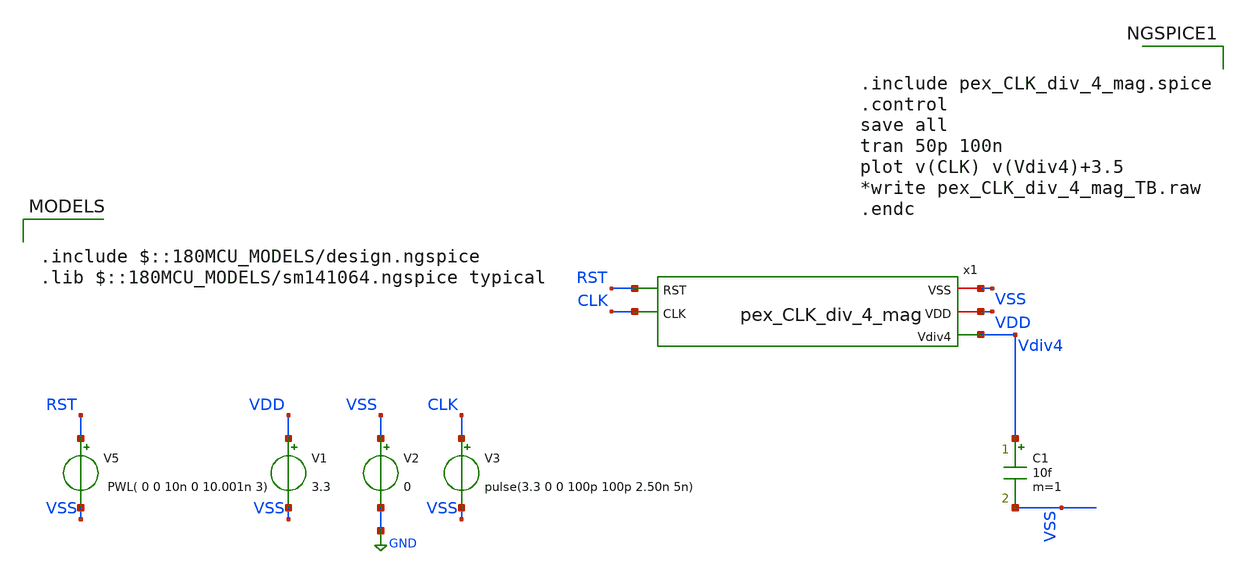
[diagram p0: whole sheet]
** sch_path: Clock_Generator_PAKISTAN_02/Schematics/pex_CLK_div_4_mag_tb.sch
**.subckt pex_CLK_div_4_mag_tb
V1 VDD VSS 3.3
V2 VSS GND 0
V3 CLK VSS pulse(3.3 0 0 100p 100p 2.50n 5n)
C1 Vdiv4 VSS 10f m=1
V5 RST VSS PWL( 0 0 10n 0 10.001n 3)
x1 VSS VDD Vdiv4 RST CLK pex_CLK_div_4_mag
**** begin user architecture code

.include $::180MCU_MODELS/design.ngspice
.lib $::180MCU_MODELS/sm141064.ngspice typical



.include pex_CLK_div_4_mag.spice
.control
save all
tran 50p 100n
plot v(CLK) v(Vdiv4)+3.5
*write pex_CLK_div_4_mag_TB.raw
.endc


**** end user architecture code
**.ends
.GLOBAL GND
.end
